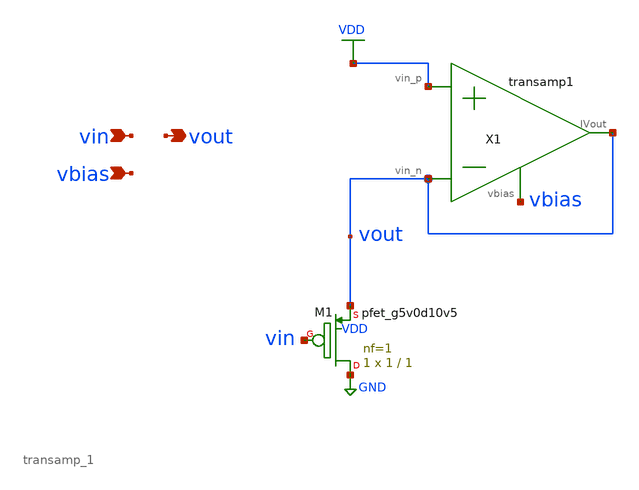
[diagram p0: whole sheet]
** sch_path: schematics/CS_amp.sch
**.subckt CS_amp vin vbias vout
*.ipin vin
*.ipin vbias
*.opin vout
XM1 GND vin vout VDD sky130_fd_pr__pfet_g5v0d10v5 L=1 W=1 nf=1 ad='int((nf+1)/2) * W/nf * 0.29' as='int((nf+2)/2) * W/nf * 0.29'
+ pd='2*int((nf+1)/2) * (W/nf + 0.29)' ps='2*int((nf+2)/2) * (W/nf + 0.29)' nrd='0.29 / W' nrs='0.29 / W'
+ sa=0 sb=0 sd=0 mult=1 m=1
X1 VDD vout vout vbias transamp_1
**.ends

* expanding   symbol:  /media/sf_share/final_project/transamp_1.sym # of pins=4
** sym_path: schematics/transamp_1.sym
** sch_path: schematics/transamp_1.sch
.subckt transamp_1 vin_p vin_n IVout vbias
*.opin IVout
*.ipin vin_p
*.ipin vin_n
*.ipin vbias
XM1 net1 vbias GND GND sky130_fd_pr__nfet_g5v0d10v5 L=1 W=1 nf=1 ad='int((nf+1)/2) * W/nf * 0.29' as='int((nf+2)/2) * W/nf * 0.29'
+ pd='2*int((nf+1)/2) * (W/nf + 0.29)' ps='2*int((nf+2)/2) * (W/nf + 0.29)' nrd='0.29 / W' nrs='0.29 / W'
+ sa=0 sb=0 sd=0 mult=1 m=1
XM3 net2 vin_p net1 GND sky130_fd_pr__nfet_g5v0d10v5 L=1 W=1 nf=1 ad='int((nf+1)/2) * W/nf * 0.29' as='int((nf+2)/2) * W/nf * 0.29'
+ pd='2*int((nf+1)/2) * (W/nf + 0.29)' ps='2*int((nf+2)/2) * (W/nf + 0.29)' nrd='0.29 / W' nrs='0.29 / W'
+ sa=0 sb=0 sd=0 mult=1 m=1
XM4 IVout net2 VDD VDD sky130_fd_pr__pfet_g5v0d10v5 L=1 W=1 nf=1 ad='int((nf+1)/2) * W/nf * 0.29' as='int((nf+2)/2) * W/nf * 0.29'
+ pd='2*int((nf+1)/2) * (W/nf + 0.29)' ps='2*int((nf+2)/2) * (W/nf + 0.29)' nrd='0.29 / W' nrs='0.29 / W'
+ sa=0 sb=0 sd=0 mult=1 m=1
XM2 IVout vin_n net1 GND sky130_fd_pr__nfet_g5v0d10v5 L=1 W=1 nf=1 ad='int((nf+1)/2) * W/nf * 0.29' as='int((nf+2)/2) * W/nf * 0.29'
+ pd='2*int((nf+1)/2) * (W/nf + 0.29)' ps='2*int((nf+2)/2) * (W/nf + 0.29)' nrd='0.29 / W' nrs='0.29 / W'
+ sa=0 sb=0 sd=0 mult=1 m=1
XM5 net2 net2 VDD VDD sky130_fd_pr__pfet_g5v0d10v5 L=1 W=1 nf=1 ad='int((nf+1)/2) * W/nf * 0.29' as='int((nf+2)/2) * W/nf * 0.29'
+ pd='2*int((nf+1)/2) * (W/nf + 0.29)' ps='2*int((nf+2)/2) * (W/nf + 0.29)' nrd='0.29 / W' nrs='0.29 / W'
+ sa=0 sb=0 sd=0 mult=1 m=1
.ends

.GLOBAL VDD
.GLOBAL GND
.end
